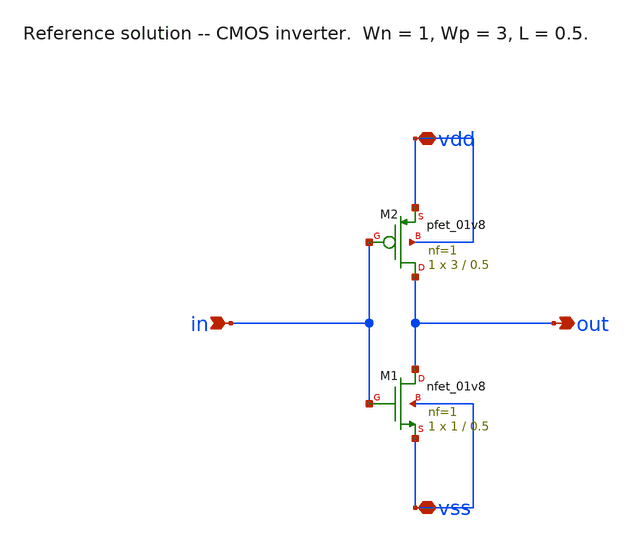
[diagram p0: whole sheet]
** sch_path: instructors/lab1/xschem/dut_inv.sch
**.subckt dut_inv in out vdd vss
*.ipin in
*.opin out
*.iopin vdd
*.iopin vss
XM2 out in vdd vdd sky130_fd_pr__pfet_01v8 L=0.5 W=3 nf=1 ad='int((nf+1)/2) * W/nf * 0.29' as='int((nf+2)/2) * W/nf * 0.29'
+ pd='2*int((nf+1)/2) * (W/nf + 0.29)' ps='2*int((nf+2)/2) * (W/nf + 0.29)' nrd='0.29 / W' nrs='0.29 / W'
+ sa=0 sb=0 sd=0 mult=1 m=1
XM1 out in vss vss sky130_fd_pr__nfet_01v8 L=0.5 W=1 nf=1 ad='int((1 + 1)/2) * 1 / 1 * 0.29' as='int((1 + 2)/2) * 1 / 1 * 0.29'
+ pd='2*int((1 + 1)/2) * (1 / 1 + 0.29)' ps='2*int((1 + 2)/2) * (1 / 1 + 0.29)' nrd='0.29 / 1 ' nrs='0.29 / 1 '
+ sa=0 sb=0 sd=0 mult=1 m=1
**.ends
.end
